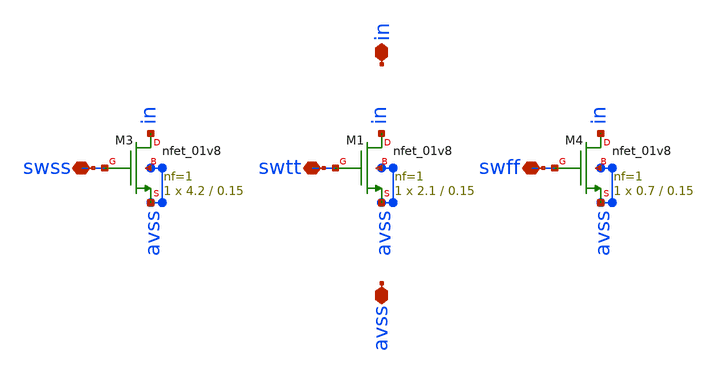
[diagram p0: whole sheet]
** sch_path: xschem/current_tails1.sch
**.subckt current_tails1 in avss swtt swff swss
*.iopin in
*.iopin avss
*.iopin swtt
*.iopin swff
*.iopin swss
XM4 in swff avss avss sky130_fd_pr__nfet_01v8 L=0.15 W=0.7 nf=1 ad='int((nf+1)/2) * W/nf * 0.29' as='int((nf+2)/2) * W/nf * 0.29'
+ pd='2*int((nf+1)/2) * (W/nf + 0.29)' ps='2*int((nf+2)/2) * (W/nf + 0.29)' nrd='0.29 / W' nrs='0.29 / W'
+ sa=0 sb=0 sd=0 mult=1 m=1
XM1 in swtt avss avss sky130_fd_pr__nfet_01v8 L=0.15 W=2.1 nf=1 ad='int((nf+1)/2) * W/nf * 0.29' as='int((nf+2)/2) * W/nf * 0.29'
+ pd='2*int((nf+1)/2) * (W/nf + 0.29)' ps='2*int((nf+2)/2) * (W/nf + 0.29)' nrd='0.29 / W' nrs='0.29 / W'
+ sa=0 sb=0 sd=0 mult=1 m=1
XM3 in swss avss avss sky130_fd_pr__nfet_01v8 L=0.15 W=4.2 nf=1 ad='int((nf+1)/2) * W/nf * 0.29' as='int((nf+2)/2) * W/nf * 0.29'
+ pd='2*int((nf+1)/2) * (W/nf + 0.29)' ps='2*int((nf+2)/2) * (W/nf + 0.29)' nrd='0.29 / W' nrs='0.29 / W'
+ sa=0 sb=0 sd=0 mult=1 m=1
**.ends
.end
